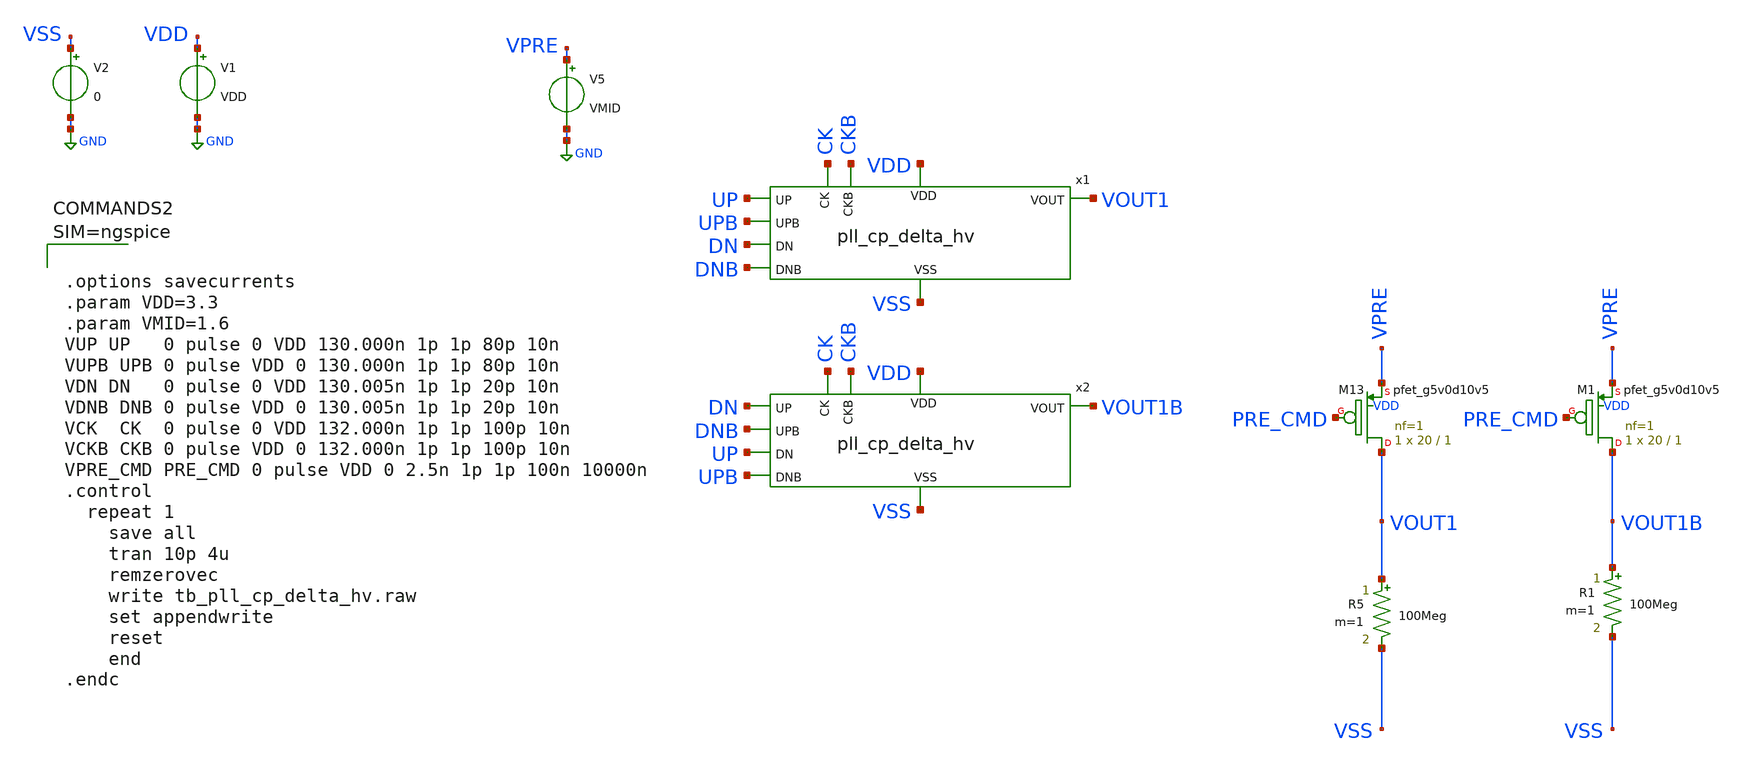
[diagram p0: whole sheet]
** sch_path: xschem/tb_pll_cp_delta_hv.sch
**.subckt tb_pll_cp_delta_hv
V1 VDD GND VDD
V2 VSS GND 0
V5 VPRE GND VMID
x1 VDD UP DN VOUT1 VSS UPB DNB CK CKB pll_cp_delta_hv
R5 VOUT1 VSS 100Meg m=1
R1 VOUT1B VSS 100Meg m=1
x2 VDD DN UP VOUT1B VSS DNB UPB CK CKB pll_cp_delta_hv
XM13 VOUT1 PRE_CMD VPRE VDD sky130_fd_pr__pfet_g5v0d10v5 L=1 W=20 nf=1 ad='int((nf+1)/2) * W/nf * 0.29'
+ as='int((nf+2)/2) * W/nf * 0.29' pd='2*int((nf+1)/2) * (W/nf + 0.29)' ps='2*int((nf+2)/2) * (W/nf + 0.29)'
+ nrd='0.29 / W' nrs='0.29 / W' sa=0 sb=0 sd=0 mult=1 m=1
XM1 VOUT1B PRE_CMD VPRE VDD sky130_fd_pr__pfet_g5v0d10v5 L=1 W=20 nf=1 ad='int((nf+1)/2) * W/nf * 0.29'
+ as='int((nf+2)/2) * W/nf * 0.29' pd='2*int((nf+1)/2) * (W/nf + 0.29)' ps='2*int((nf+2)/2) * (W/nf + 0.29)'
+ nrd='0.29 / W' nrs='0.29 / W' sa=0 sb=0 sd=0 mult=1 m=1
**** begin user architecture code

** opencircuitdesign pdks install
.lib $::SKYWATER_MODELS/sky130.lib.spice tt





.options savecurrents
.param VDD=3.3
.param VMID=1.6
VUP UP   0 pulse 0 VDD 130.000n 1p 1p 80p 10n
VUPB UPB 0 pulse VDD 0 130.000n 1p 1p 80p 10n
VDN DN   0 pulse 0 VDD 130.005n 1p 1p 20p 10n
VDNB DNB 0 pulse VDD 0 130.005n 1p 1p 20p 10n
VCK  CK  0 pulse 0 VDD 132.000n 1p 1p 100p 10n
VCKB CKB 0 pulse VDD 0 132.000n 1p 1p 100p 10n
VPRE_CMD PRE_CMD 0 pulse VDD 0 2.5n 1p 1p 100n 10000n
.control
  repeat 1
    save all
    tran 10p 4u
    remzerovec
    write tb_pll_cp_delta_hv.raw
    set appendwrite
    reset
    end
.endc



**** end user architecture code
**.ends

* expanding   symbol:  pll_cp_delta_hv.sym # of pins=9
** sym_path: xschem/pll_cp_delta_hv.sym
** sch_path: xschem/pll_cp_delta_hv.sch
.subckt pll_cp_delta_hv VDD UP DN VOUT VSS UPB DNB CK CKB
*.opin VOUT
*.ipin VSS
*.ipin UP
*.ipin DNB
*.ipin CK
*.ipin CKB
*.ipin VDD
*.ipin DN
*.ipin UPB
XC1 VOUT VSS sky130_fd_pr__cap_mim_m3_1 W=30 L=30 MF=1 m=1
vibias net3 net6 0
.save i(vibias)
XM16 net9 net2 VDD VDD sky130_fd_pr__pfet_g5v0d10v5 L=1 W=3 nf=1 ad='int((nf+1)/2) * W/nf * 0.29' as='int((nf+2)/2) * W/nf * 0.29'
+ pd='2*int((nf+1)/2) * (W/nf + 0.29)' ps='2*int((nf+2)/2) * (W/nf + 0.29)' nrd='0.29 / W' nrs='0.29 / W'
+ sa=0 sb=0 sd=0 mult=1 m=1
XM13 net2 net2 VDD VDD sky130_fd_pr__pfet_g5v0d10v5 L=1 W=2 nf=1 ad='int((nf+1)/2) * W/nf * 0.29' as='int((nf+2)/2) * W/nf * 0.29'
+ pd='2*int((nf+1)/2) * (W/nf + 0.29)' ps='2*int((nf+2)/2) * (W/nf + 0.29)' nrd='0.29 / W' nrs='0.29 / W'
+ sa=0 sb=0 sd=0 mult=1 m=1
XM14 net3 net3 net2 VDD sky130_fd_pr__pfet_g5v0d10v5 L=1 W=2 nf=1 ad='int((nf+1)/2) * W/nf * 0.29' as='int((nf+2)/2) * W/nf * 0.29'
+ pd='2*int((nf+1)/2) * (W/nf + 0.29)' ps='2*int((nf+2)/2) * (W/nf + 0.29)' nrd='0.29 / W' nrs='0.29 / W'
+ sa=0 sb=0 sd=0 mult=1 m=1
I0 VDD net4 200u
XM11 net1 net1 VSS VSS sky130_fd_pr__nfet_g5v0d10v5 L=1 W=2 nf=1 ad='int((nf+1)/2) * W/nf * 0.29' as='int((nf+2)/2) * W/nf * 0.29'
+ pd='2*int((nf+1)/2) * (W/nf + 0.29)' ps='2*int((nf+2)/2) * (W/nf + 0.29)' nrd='0.29 / W' nrs='0.29 / W'
+ sa=0 sb=0 sd=0 mult=1 m=1
XM17 net4 net4 net1 VSS sky130_fd_pr__nfet_g5v0d10v5 L=1 W=2 nf=1 ad='int((nf+1)/2) * W/nf * 0.29' as='int((nf+2)/2) * W/nf * 0.29'
+ pd='2*int((nf+1)/2) * (W/nf + 0.29)' ps='2*int((nf+2)/2) * (W/nf + 0.29)' nrd='0.29 / W' nrs='0.29 / W'
+ sa=0 sb=0 sd=0 mult=1 m=1
XM15 net5 net1 VSS VSS sky130_fd_pr__nfet_g5v0d10v5 L=1 W=2 nf=1 ad='int((nf+1)/2) * W/nf * 0.29' as='int((nf+2)/2) * W/nf * 0.29'
+ pd='2*int((nf+1)/2) * (W/nf + 0.29)' ps='2*int((nf+2)/2) * (W/nf + 0.29)' nrd='0.29 / W' nrs='0.29 / W'
+ sa=0 sb=0 sd=0 mult=1 m=1
XM18 net6 net4 net5 VSS sky130_fd_pr__nfet_g5v0d10v5 L=1 W=2 nf=1 ad='int((nf+1)/2) * W/nf * 0.29' as='int((nf+2)/2) * W/nf * 0.29'
+ pd='2*int((nf+1)/2) * (W/nf + 0.29)' ps='2*int((nf+2)/2) * (W/nf + 0.29)' nrd='0.29 / W' nrs='0.29 / W'
+ sa=0 sb=0 sd=0 mult=1 m=1
XM6 net7 net1 VSS VSS sky130_fd_pr__nfet_g5v0d10v5 L=1 W=2 nf=1 ad='int((nf+1)/2) * W/nf * 0.29' as='int((nf+2)/2) * W/nf * 0.29'
+ pd='2*int((nf+1)/2) * (W/nf + 0.29)' ps='2*int((nf+2)/2) * (W/nf + 0.29)' nrd='0.29 / W' nrs='0.29 / W'
+ sa=0 sb=0 sd=0 mult=1 m=1
XM19 net8 net4 net7 VSS sky130_fd_pr__nfet_g5v0d10v5 L=1 W=2 nf=1 ad='int((nf+1)/2) * W/nf * 0.29' as='int((nf+2)/2) * W/nf * 0.29'
+ pd='2*int((nf+1)/2) * (W/nf + 0.29)' ps='2*int((nf+2)/2) * (W/nf + 0.29)' nrd='0.29 / W' nrs='0.29 / W'
+ sa=0 sb=0 sd=0 mult=1 m=1
XM20 net11 DN net8 VSS sky130_fd_pr__nfet_g5v0d10v5 L=0.5 W=1 nf=1 ad='int((nf+1)/2) * W/nf * 0.29' as='int((nf+2)/2) * W/nf * 0.29'
+ pd='2*int((nf+1)/2) * (W/nf + 0.29)' ps='2*int((nf+2)/2) * (W/nf + 0.29)' nrd='0.29 / W' nrs='0.29 / W'
+ sa=0 sb=0 sd=0 mult=1 m=1
XM4 net10 net3 net9 VDD sky130_fd_pr__pfet_g5v0d10v5 L=1 W=3 nf=1 ad='int((nf+1)/2) * W/nf * 0.29' as='int((nf+2)/2) * W/nf * 0.29'
+ pd='2*int((nf+1)/2) * (W/nf + 0.29)' ps='2*int((nf+2)/2) * (W/nf + 0.29)' nrd='0.29 / W' nrs='0.29 / W'
+ sa=0 sb=0 sd=0 mult=1 m=1
viup net12 VOUT 0
.save i(viup)
vidown VOUT net11 0
.save i(vidown)
XM1 net12 UPB net10 VDD sky130_fd_pr__pfet_g5v0d10v5 L=1 W=3 nf=1 ad='int((nf+1)/2) * W/nf * 0.29' as='int((nf+2)/2) * W/nf * 0.29'
+ pd='2*int((nf+1)/2) * (W/nf + 0.29)' ps='2*int((nf+2)/2) * (W/nf + 0.29)' nrd='0.29 / W' nrs='0.29 / W'
+ sa=0 sb=0 sd=0 mult=1 m=1
.ends

.GLOBAL GND
.end
